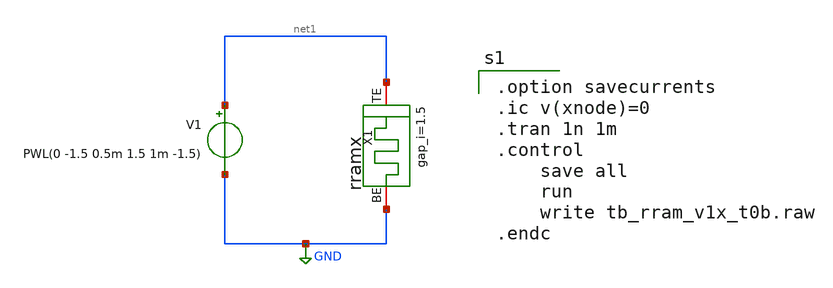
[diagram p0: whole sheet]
** sch_path: designs/tb_memristor/tb_rram_v1x_t0b.sch
**.subckt tb_rram_v1x_t0b
V1 net1 GND PWL(0 -1.5 0.5m 1.5 1m -1.5)
.save i(v1)
X1 net1 GND rram_cell gap_i=1.5
**** begin user architecture code

.option savecurrents
.ic v(xnode)=0
.tran 1n 1m
.control
	save all
	run
	write tb_rram_v1x_t0b.raw
.endc


.subckt rram_cell BE TE gap_i=0.1
N1 BE TE rram_model
.model rram_model rram  gap_initial=1
.ends rram_cell

.control
pre_osdi /foss/designs/spike_130/designs/memristors/rram_v1/rram.osdi
.endc

**** end user architecture code
**.ends
.GLOBAL GND
.end
